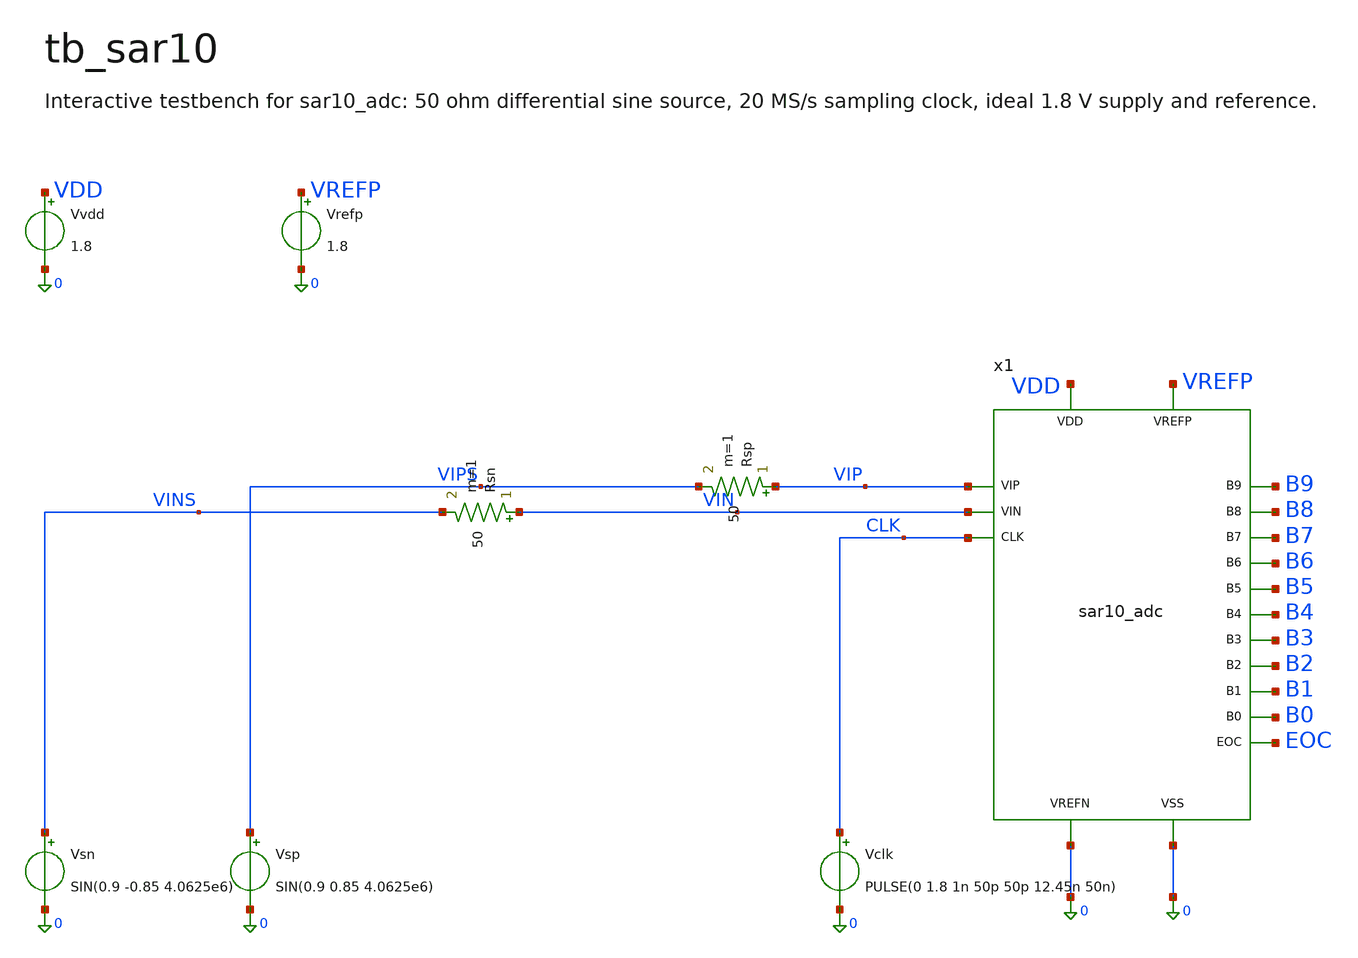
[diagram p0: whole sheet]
** sch_path: xschem/tb_sar10.sch
**.subckt tb_sar10
x1 VIP VIN CLK B9 B8 B7 B6 B5 B4 B3 B2 B1 B0 EOC VDD VREFP 0 0 sar10_adc
Rsp VIP VIPS 50 m=1
Rsn VIN VINS 50 m=1
Vsp VIPS 0 SIN(0.9 0.85 4.0625e6)
Vsn VINS 0 SIN(0.9 -0.85 4.0625e6)
Vclk CLK 0 PULSE(0 1.8 1n 50p 50p 12.45n 50n)
Vvdd VDD 0 1.8
.save i(vvdd)
Vrefp VREFP 0 1.8
.save i(vrefp)
**** begin user architecture code

* sar10_adc bench: 16 conversions of a 4.0625 MHz sine at 20 MS/s (CLK high = sample).
* Netlist + Simulate from xschem.  Corner on the .lib line, temperature on .temp.
* For ENOB / corners / power use the flow instead:  python3 gen/flow.py fft --out sim/x --N 256 --M
*+ 31

.lib /foss/pdks/sky130A/libs.tech/ngspice/sky130.lib.spice tt
.include /foss/pdks/sky130A/libs.ref/sky130_fd_sc_hd/spice/sky130_fd_sc_hd.spice
.include /foss/pdks/sky130A/libs.ref/sky130_fd_pr/spice/sky130_fd_pr__cap_vpp_01p8x01p8_m1m2_noshield.model.spice
.temp 27
.option reltol=2e-4 abstol=1e-13 vntol=1e-7 chgtol=1e-16 method=gear klu rshunt=1e15
.save v(vip) v(vin) v(clk) v(eoc) v(b9) v(b8) v(b7) v(b6) v(b5) v(b4) v(b3) v(b2) v(b1) v(b0)
.save v(x1.topp) v(x1.topn) v(x1.clkc) v(x1.outp) v(x1.outn) i(vvdd) i(vrefp)
.tran 20p 851n 0 40p uic

.control
  run
  let msbs = 512*(v(b9) gt 0.9) + 256*(v(b8) gt 0.9) + 128*(v(b7) gt 0.9) + 64*(v(b6) gt 0.9) +
+ 32*(v(b5) gt 0.9)
  let code = msbs + 16*(v(b4) gt 0.9) + 8*(v(b3) gt 0.9) + 4*(v(b2) gt 0.9) + 2*(v(b1) gt 0.9) +
+ (v(b0) gt 0.9)
  let vd = v(vip) - v(vin)
  meas tran i_vdd AVG i(vvdd) FROM=51n TO=851n
  meas tran i_ref AVG i(vrefp) FROM=51n TO=851n
  let p_uw = -1.8e6*(i_vdd + i_ref)
  echo total power $&p_uw uW at 20 MS/s
  plot code
  plot vd v(eoc) v(clk)
  plot v(x1.topp) v(x1.topn) v(x1.clkc) xlimit 60n 80n
.endc


**** end user architecture code
**.ends

* expanding   symbol:  sar10_adc.sym # of pins=18
** sym_path: xschem/sar10_adc.sym
** sch_path: xschem/sar10_adc.sch
.subckt sar10_adc VIP VIN CLK B9 B8 B7 B6 B5 B4 B3 B2 B1 B0 EOC VDD VREFP VREFN VSS
*.ipin VIP
*.ipin VIN
*.ipin CLK
*.opin EOC
*.opin B9
*.opin B8
*.opin B7
*.opin B6
*.opin B5
*.opin B4
*.opin B3
*.opin B2
*.opin B1
*.opin B0
*.iopin VDD
*.iopin VREFP
*.iopin VREFN
*.iopin VSS
* noconn #net1
* noconn #net2
* noconn #net3
* noconn #net4
* noconn #net5
* noconn #net6
* noconn #net7
* noconn #net8
* noconn #net9
* noconn #net10
* noconn #net11
* noconn #net12
* noconn #net13
XBSP VIP TOPP VDD SAMP VSS sar10_boot
XBSN VIN TOPN VDD SAMP VSS sar10_boot
XDP1 DP1 DNB1 TOPP VDD VREFP VREFN VSS sar10_dac128
XDN1 DN1 DPB1 TOPN VDD VREFP VREFN VSS sar10_dac128
XDP2 DP2 DNB2 TOPP VDD VREFP VREFN VSS sar10_dac64
XDN2 DN2 DPB2 TOPN VDD VREFP VREFN VSS sar10_dac64
XDP3 DP3 DNB3 TOPP VDD VREFP VREFN VSS sar10_dac32
XDN3 DN3 DPB3 TOPN VDD VREFP VREFN VSS sar10_dac32
XDP4 DP4 DNB4 TOPP VDD VREFP VREFN VSS sar10_dac16
XDN4 DN4 DPB4 TOPN VDD VREFP VREFN VSS sar10_dac16
XDP5 DP5 DNB5 TOPP VDD VREFP VREFN VSS sar10_dac8
XDN5 DN5 DPB5 TOPN VDD VREFP VREFN VSS sar10_dac8
XDP6 DP6 DNB6 TOPP VDD VREFP VREFN VSS sar10_dac4
XDN6 DN6 DPB6 TOPN VDD VREFP VREFN VSS sar10_dac4
XDP7 DP7 DNB7 TOPP VDD VREFP VREFN VSS sar10_dac2
XDN7 DN7 DPB7 TOPN VDD VREFP VREFN VSS sar10_dac2
XDP8 DP8 DNB8 TOPP VDD VREFP VREFN VSS sar10_dac1
XDN8 DN8 DPB8 TOPN VDD VREFP VREFN VSS sar10_dac1
XDP9 DP9 DNB9 TOPP VDD VREFP VREFN VSS sar10_dac1
XDN9 TOPN VREFP VREFN VSS sar10_dacdum
XCMP TOPP TOPN CLKC OUTP OUTN VDD VSS sar10_comp
XCTL OUTP OUTN CLK DEC10 CLKC QP QN VALIDB RSTB SAMP EOC VDD VSS sar10_ctrl
XS1 RSTB QP QN VALIDB RSTB EOC T1 net1 DP1 DPB1 DN1 DNB1 B9 VDD VSS sar10_slice
XS2 T1 QP QN VALIDB RSTB EOC T2 net2 DP2 DPB2 DN2 DNB2 B8 VDD VSS sar10_slice
XS3 T2 QP QN VALIDB RSTB EOC T3 net3 DP3 DPB3 DN3 DNB3 B7 VDD VSS sar10_slice
XS4 T3 QP QN VALIDB RSTB EOC T4 net4 DP4 DPB4 DN4 DNB4 B6 VDD VSS sar10_slice
XS5 T4 QP QN VALIDB RSTB EOC T5 net5 DP5 DPB5 DN5 DNB5 B5 VDD VSS sar10_slice
XS6 T5 QP QN VALIDB RSTB EOC T6 net6 DP6 DPB6 DN6 DNB6 B4 VDD VSS sar10_slice
XS7 T6 QP QN VALIDB RSTB EOC T7 net7 DP7 DPB7 DN7 DNB7 B3 VDD VSS sar10_slice
XS8 T7 QP QN VALIDB RSTB EOC T8 net8 DP8 DPB8 DN8 DNB8 B2 VDD VSS sar10_slice
XS9 T8 QP QN VALIDB RSTB EOC T9 net9 DP9 DPB9 DN9 DNB9 B1 VDD VSS sar10_slice
XS10 T9 QP QN VALIDB RSTB EOC net13 DEC10 DP10 net10 net11 net12 B0 VDD VSS sar10_slice
.ends


* expanding   symbol:  sar10_boot.sym # of pins=5
** sym_path: xschem/sar10_boot.sym
** sch_path: xschem/sar10_boot.sch
.subckt sar10_boot VIN VOUT VDD CK VSS
*.ipin CK
*.ipin VIN
*.opin VOUT
*.iopin VDD
*.iopin VSS
XMPI CKB CK VDD VDD sky130_fd_pr__pfet_01v8 L=0.15 W=6 nf=1 ad='int((1 + 1)/2) * 6 / 1 * 0.29' as='int((1 + 2)/2) * 6 / 1 * 0.29'
+ pd='2*int((1 + 1)/2) * (6 / 1 + 0.29)' ps='2*int((1 + 2)/2) * (6 / 1 + 0.29)' nrd='0.29 / 6 ' nrs='0.29 / 6 '
+ sa=0 sb=0 sd=0 mult=1 m=1
XMNI CKB CK VSS VSS sky130_fd_pr__nfet_01v8 L=0.15 W=3 nf=1 ad='int((1 + 1)/2) * 3 / 1 * 0.29' as='int((1 + 2)/2) * 3 / 1 * 0.29'
+ pd='2*int((1 + 1)/2) * (3 / 1 + 0.29)' ps='2*int((1 + 2)/2) * (3 / 1 + 0.29)' nrd='0.29 / 3 ' nrs='0.29 / 3 '
+ sa=0 sb=0 sd=0 mult=1 m=1
XMP1 TOP G VDD TOP sky130_fd_pr__pfet_01v8 L=0.15 W=2 nf=1 ad='int((1 + 1)/2) * 2 / 1 * 0.29' as='int((1 + 2)/2) * 2 / 1 * 0.29'
+ pd='2*int((1 + 1)/2) * (2 / 1 + 0.29)' ps='2*int((1 + 2)/2) * (2 / 1 + 0.29)' nrd='0.29 / 2 ' nrs='0.29 / 2 '
+ sa=0 sb=0 sd=0 mult=1 m=1
XCB TOP BOT sky130_fd_pr__cap_mim_m3_1 W=9 L=9 MF=1 m=1
XMN1 BOT CKB VSS VSS sky130_fd_pr__nfet_01v8 L=0.15 W=2 nf=1 ad='int((1 + 1)/2) * 2 / 1 * 0.29' as='int((1 + 2)/2) * 2 / 1 * 0.29'
+ pd='2*int((1 + 1)/2) * (2 / 1 + 0.29)' ps='2*int((1 + 2)/2) * (2 / 1 + 0.29)' nrd='0.29 / 2 ' nrs='0.29 / 2 '
+ sa=0 sb=0 sd=0 mult=1 m=1
XMP4 Z CK VDD VDD sky130_fd_pr__pfet_01v8 L=0.15 W=6 nf=1 ad='int((1 + 1)/2) * 6 / 1 * 0.29' as='int((1 + 2)/2) * 6 / 1 * 0.29'
+ pd='2*int((1 + 1)/2) * (6 / 1 + 0.29)' ps='2*int((1 + 2)/2) * (6 / 1 + 0.29)' nrd='0.29 / 6 ' nrs='0.29 / 6 '
+ sa=0 sb=0 sd=0 mult=1 m=1
XMN4 Z CK BOT VSS sky130_fd_pr__nfet_01v8 L=0.15 W=1 nf=1 ad='int((1 + 1)/2) * 1 / 1 * 0.29' as='int((1 + 2)/2) * 1 / 1 * 0.29'
+ pd='2*int((1 + 1)/2) * (1 / 1 + 0.29)' ps='2*int((1 + 2)/2) * (1 / 1 + 0.29)' nrd='0.29 / 1 ' nrs='0.29 / 1 '
+ sa=0 sb=0 sd=0 mult=1 m=1
XMN4B Z G BOT VSS sky130_fd_pr__nfet_01v8 L=0.15 W=1 nf=1 ad='int((1 + 1)/2) * 1 / 1 * 0.29' as='int((1 + 2)/2) * 1 / 1 * 0.29'
+ pd='2*int((1 + 1)/2) * (1 / 1 + 0.29)' ps='2*int((1 + 2)/2) * (1 / 1 + 0.29)' nrd='0.29 / 1 ' nrs='0.29 / 1 '
+ sa=0 sb=0 sd=0 mult=1 m=1
XMP2 G Z TOP TOP sky130_fd_pr__pfet_01v8 L=0.15 W=4 nf=1 ad='int((1 + 1)/2) * 4 / 1 * 0.29' as='int((1 + 2)/2) * 4 / 1 * 0.29'
+ pd='2*int((1 + 1)/2) * (4 / 1 + 0.29)' ps='2*int((1 + 2)/2) * (4 / 1 + 0.29)' nrd='0.29 / 4 ' nrs='0.29 / 4 '
+ sa=0 sb=0 sd=0 mult=1 m=1
XMN3 BOT G VIN VSS sky130_fd_pr__nfet_01v8 L=0.15 W=4 nf=1 ad='int((1 + 1)/2) * 4 / 1 * 0.29' as='int((1 + 2)/2) * 4 / 1 * 0.29'
+ pd='2*int((1 + 1)/2) * (4 / 1 + 0.29)' ps='2*int((1 + 2)/2) * (4 / 1 + 0.29)' nrd='0.29 / 4 ' nrs='0.29 / 4 '
+ sa=0 sb=0 sd=0 mult=1 m=1
XMN2A G VDD GX VSS sky130_fd_pr__nfet_01v8 L=0.15 W=12 nf=1 ad='int((1 + 1)/2) * 12 / 1 * 0.29' as='int((1 + 2)/2) * 12 / 1 * 0.29'
+ pd='2*int((1 + 1)/2) * (12 / 1 + 0.29)' ps='2*int((1 + 2)/2) * (12 / 1 + 0.29)' nrd='0.29 / 12 ' nrs='0.29 / 12 '
+ sa=0 sb=0 sd=0 mult=1 m=1
XMN2 GX CKB VSS VSS sky130_fd_pr__nfet_01v8 L=0.15 W=12 nf=1 ad='int((1 + 1)/2) * 12 / 1 * 0.29' as='int((1 + 2)/2) * 12 / 1 * 0.29'
+ pd='2*int((1 + 1)/2) * (12 / 1 + 0.29)' ps='2*int((1 + 2)/2) * (12 / 1 + 0.29)' nrd='0.29 / 12 ' nrs='0.29 / 12 '
+ sa=0 sb=0 sd=0 mult=1 m=1
XMSW VOUT G VIN VSS sky130_fd_pr__nfet_01v8 L=0.15 W=5 nf=2 ad='int((2 + 1)/2) * 5 / 2 * 0.29' as='int((2 + 2)/2) * 5 / 2 * 0.29'
+ pd='2*int((2 + 1)/2) * (5 / 2 + 0.29)' ps='2*int((2 + 2)/2) * (5 / 2 + 0.29)' nrd='0.29 / 5 ' nrs='0.29 / 5 '
+ sa=0 sb=0 sd=0 mult=1 m=1
.ends


* expanding   symbol:  sar10_dac128.sym # of pins=7
** sym_path: xschem/sar10_dac128.sym
** sch_path: xschem/sar10_dac128.sch
.subckt sar10_dac128 DH DL TOP VDD VREFP VREFN VSS
*.ipin DH
*.ipin DL
*.iopin TOP
*.iopin VDD
*.iopin VREFP
*.iopin VREFN
*.iopin VSS
XMP3H BH DH VREFP VREFP sky130_fd_pr__pfet_01v8 L=0.15 W=14.4 nf=3 ad='int((3 + 1)/2) * 14.4 / 3 * 0.29'
+ as='int((3 + 2)/2) * 14.4 / 3 * 0.29' pd='2*int((3 + 1)/2) * (14.4 / 3 + 0.29)' ps='2*int((3 + 2)/2) * (14.4 / 3 + 0.29)'
+ nrd='0.29 / 14.4 ' nrs='0.29 / 14.4 ' sa=0 sb=0 sd=0 mult=1 m=1
XMN3H BH DH VREFN VREFN sky130_fd_pr__nfet_01v8 L=0.15 W=5.76 nf=2 ad='int((2 + 1)/2) * 5.76 / 2 * 0.29'
+ as='int((2 + 2)/2) * 5.76 / 2 * 0.29' pd='2*int((2 + 1)/2) * (5.76 / 2 + 0.29)' ps='2*int((2 + 2)/2) * (5.76 / 2 + 0.29)'
+ nrd='0.29 / 5.76 ' nrs='0.29 / 5.76 ' sa=0 sb=0 sd=0 mult=1 m=1
XMP3L BL DL VREFP VREFP sky130_fd_pr__pfet_01v8 L=0.15 W=14.4 nf=3 ad='int((3 + 1)/2) * 14.4 / 3 * 0.29'
+ as='int((3 + 2)/2) * 14.4 / 3 * 0.29' pd='2*int((3 + 1)/2) * (14.4 / 3 + 0.29)' ps='2*int((3 + 2)/2) * (14.4 / 3 + 0.29)'
+ nrd='0.29 / 14.4 ' nrs='0.29 / 14.4 ' sa=0 sb=0 sd=0 mult=1 m=1
XMN3L BL DL VREFN VREFN sky130_fd_pr__nfet_01v8 L=0.15 W=5.76 nf=2 ad='int((2 + 1)/2) * 5.76 / 2 * 0.29'
+ as='int((2 + 2)/2) * 5.76 / 2 * 0.29' pd='2*int((2 + 1)/2) * (5.76 / 2 + 0.29)' ps='2*int((2 + 2)/2) * (5.76 / 2 + 0.29)'
+ nrd='0.29 / 5.76 ' nrs='0.29 / 5.76 ' sa=0 sb=0 sd=0 mult=1 m=1
XCH BH TOP VSS sky130_fd_pr__cap_vpp_01p8x01p8_m1m2_noshield mult=128 m=128
XCL BL TOP VSS sky130_fd_pr__cap_vpp_01p8x01p8_m1m2_noshield mult=128 m=128
.ends


* expanding   symbol:  sar10_dac64.sym # of pins=7
** sym_path: xschem/sar10_dac64.sym
** sch_path: xschem/sar10_dac64.sch
.subckt sar10_dac64 DH DL TOP VDD VREFP VREFN VSS
*.ipin DH
*.ipin DL
*.iopin TOP
*.iopin VDD
*.iopin VREFP
*.iopin VREFN
*.iopin VSS
XMP3H BH DH VREFP VREFP sky130_fd_pr__pfet_01v8 L=0.15 W=7.2 nf=2 ad='int((2 + 1)/2) * 7.2 / 2 * 0.29'
+ as='int((2 + 2)/2) * 7.2 / 2 * 0.29' pd='2*int((2 + 1)/2) * (7.2 / 2 + 0.29)' ps='2*int((2 + 2)/2) * (7.2 / 2 + 0.29)'
+ nrd='0.29 / 7.2 ' nrs='0.29 / 7.2 ' sa=0 sb=0 sd=0 mult=1 m=1
XMN3H BH DH VREFN VREFN sky130_fd_pr__nfet_01v8 L=0.15 W=2.88 nf=1 ad='int((1 + 1)/2) * 2.88 / 1 * 0.29'
+ as='int((1 + 2)/2) * 2.88 / 1 * 0.29' pd='2*int((1 + 1)/2) * (2.88 / 1 + 0.29)' ps='2*int((1 + 2)/2) * (2.88 / 1 + 0.29)'
+ nrd='0.29 / 2.88 ' nrs='0.29 / 2.88 ' sa=0 sb=0 sd=0 mult=1 m=1
XMP3L BL DL VREFP VREFP sky130_fd_pr__pfet_01v8 L=0.15 W=7.2 nf=2 ad='int((2 + 1)/2) * 7.2 / 2 * 0.29'
+ as='int((2 + 2)/2) * 7.2 / 2 * 0.29' pd='2*int((2 + 1)/2) * (7.2 / 2 + 0.29)' ps='2*int((2 + 2)/2) * (7.2 / 2 + 0.29)'
+ nrd='0.29 / 7.2 ' nrs='0.29 / 7.2 ' sa=0 sb=0 sd=0 mult=1 m=1
XMN3L BL DL VREFN VREFN sky130_fd_pr__nfet_01v8 L=0.15 W=2.88 nf=1 ad='int((1 + 1)/2) * 2.88 / 1 * 0.29'
+ as='int((1 + 2)/2) * 2.88 / 1 * 0.29' pd='2*int((1 + 1)/2) * (2.88 / 1 + 0.29)' ps='2*int((1 + 2)/2) * (2.88 / 1 + 0.29)'
+ nrd='0.29 / 2.88 ' nrs='0.29 / 2.88 ' sa=0 sb=0 sd=0 mult=1 m=1
XCH BH TOP VSS sky130_fd_pr__cap_vpp_01p8x01p8_m1m2_noshield mult=64 m=64
XCL BL TOP VSS sky130_fd_pr__cap_vpp_01p8x01p8_m1m2_noshield mult=64 m=64
.ends


* expanding   symbol:  sar10_dac32.sym # of pins=7
** sym_path: xschem/sar10_dac32.sym
** sch_path: xschem/sar10_dac32.sch
.subckt sar10_dac32 DH DL TOP VDD VREFP VREFN VSS
*.ipin DH
*.ipin DL
*.iopin TOP
*.iopin VDD
*.iopin VREFP
*.iopin VREFN
*.iopin VSS
XMP3H BH DH VREFP VREFP sky130_fd_pr__pfet_01v8 L=0.15 W=3.6 nf=1 ad='int((1 + 1)/2) * 3.6 / 1 * 0.29'
+ as='int((1 + 2)/2) * 3.6 / 1 * 0.29' pd='2*int((1 + 1)/2) * (3.6 / 1 + 0.29)' ps='2*int((1 + 2)/2) * (3.6 / 1 + 0.29)'
+ nrd='0.29 / 3.6 ' nrs='0.29 / 3.6 ' sa=0 sb=0 sd=0 mult=1 m=1
XMN3H BH DH VREFN VREFN sky130_fd_pr__nfet_01v8 L=0.15 W=1.44 nf=1 ad='int((1 + 1)/2) * 1.44 / 1 * 0.29'
+ as='int((1 + 2)/2) * 1.44 / 1 * 0.29' pd='2*int((1 + 1)/2) * (1.44 / 1 + 0.29)' ps='2*int((1 + 2)/2) * (1.44 / 1 + 0.29)'
+ nrd='0.29 / 1.44 ' nrs='0.29 / 1.44 ' sa=0 sb=0 sd=0 mult=1 m=1
XMP3L BL DL VREFP VREFP sky130_fd_pr__pfet_01v8 L=0.15 W=3.6 nf=1 ad='int((1 + 1)/2) * 3.6 / 1 * 0.29'
+ as='int((1 + 2)/2) * 3.6 / 1 * 0.29' pd='2*int((1 + 1)/2) * (3.6 / 1 + 0.29)' ps='2*int((1 + 2)/2) * (3.6 / 1 + 0.29)'
+ nrd='0.29 / 3.6 ' nrs='0.29 / 3.6 ' sa=0 sb=0 sd=0 mult=1 m=1
XMN3L BL DL VREFN VREFN sky130_fd_pr__nfet_01v8 L=0.15 W=1.44 nf=1 ad='int((1 + 1)/2) * 1.44 / 1 * 0.29'
+ as='int((1 + 2)/2) * 1.44 / 1 * 0.29' pd='2*int((1 + 1)/2) * (1.44 / 1 + 0.29)' ps='2*int((1 + 2)/2) * (1.44 / 1 + 0.29)'
+ nrd='0.29 / 1.44 ' nrs='0.29 / 1.44 ' sa=0 sb=0 sd=0 mult=1 m=1
XCH BH TOP VSS sky130_fd_pr__cap_vpp_01p8x01p8_m1m2_noshield mult=32 m=32
XCL BL TOP VSS sky130_fd_pr__cap_vpp_01p8x01p8_m1m2_noshield mult=32 m=32
.ends


* expanding   symbol:  sar10_dac16.sym # of pins=7
** sym_path: xschem/sar10_dac16.sym
** sch_path: xschem/sar10_dac16.sch
.subckt sar10_dac16 DH DL TOP VDD VREFP VREFN VSS
*.ipin DH
*.ipin DL
*.iopin TOP
*.iopin VDD
*.iopin VREFP
*.iopin VREFN
*.iopin VSS
XMP3H BH DH VREFP VREFP sky130_fd_pr__pfet_01v8 L=0.15 W=1.8 nf=1 ad='int((1 + 1)/2) * 1.8 / 1 * 0.29'
+ as='int((1 + 2)/2) * 1.8 / 1 * 0.29' pd='2*int((1 + 1)/2) * (1.8 / 1 + 0.29)' ps='2*int((1 + 2)/2) * (1.8 / 1 + 0.29)'
+ nrd='0.29 / 1.8 ' nrs='0.29 / 1.8 ' sa=0 sb=0 sd=0 mult=1 m=1
XMN3H BH DH VREFN VREFN sky130_fd_pr__nfet_01v8 L=0.15 W=0.72 nf=1 ad='int((1 + 1)/2) * 0.72 / 1 * 0.29'
+ as='int((1 + 2)/2) * 0.72 / 1 * 0.29' pd='2*int((1 + 1)/2) * (0.72 / 1 + 0.29)' ps='2*int((1 + 2)/2) * (0.72 / 1 + 0.29)'
+ nrd='0.29 / 0.72 ' nrs='0.29 / 0.72 ' sa=0 sb=0 sd=0 mult=1 m=1
XMP3L BL DL VREFP VREFP sky130_fd_pr__pfet_01v8 L=0.15 W=1.8 nf=1 ad='int((1 + 1)/2) * 1.8 / 1 * 0.29'
+ as='int((1 + 2)/2) * 1.8 / 1 * 0.29' pd='2*int((1 + 1)/2) * (1.8 / 1 + 0.29)' ps='2*int((1 + 2)/2) * (1.8 / 1 + 0.29)'
+ nrd='0.29 / 1.8 ' nrs='0.29 / 1.8 ' sa=0 sb=0 sd=0 mult=1 m=1
XMN3L BL DL VREFN VREFN sky130_fd_pr__nfet_01v8 L=0.15 W=0.72 nf=1 ad='int((1 + 1)/2) * 0.72 / 1 * 0.29'
+ as='int((1 + 2)/2) * 0.72 / 1 * 0.29' pd='2*int((1 + 1)/2) * (0.72 / 1 + 0.29)' ps='2*int((1 + 2)/2) * (0.72 / 1 + 0.29)'
+ nrd='0.29 / 0.72 ' nrs='0.29 / 0.72 ' sa=0 sb=0 sd=0 mult=1 m=1
XCH BH TOP VSS sky130_fd_pr__cap_vpp_01p8x01p8_m1m2_noshield mult=16 m=16
XCL BL TOP VSS sky130_fd_pr__cap_vpp_01p8x01p8_m1m2_noshield mult=16 m=16
.ends


* expanding   symbol:  sar10_dac8.sym # of pins=7
** sym_path: xschem/sar10_dac8.sym
** sch_path: xschem/sar10_dac8.sch
.subckt sar10_dac8 DH DL TOP VDD VREFP VREFN VSS
*.ipin DH
*.ipin DL
*.iopin TOP
*.iopin VDD
*.iopin VREFP
*.iopin VREFN
*.iopin VSS
XMP3H BH DH VREFP VREFP sky130_fd_pr__pfet_01v8 L=0.15 W=1.05 nf=1 ad='int((1 + 1)/2) * 1.05 / 1 * 0.29'
+ as='int((1 + 2)/2) * 1.05 / 1 * 0.29' pd='2*int((1 + 1)/2) * (1.05 / 1 + 0.29)' ps='2*int((1 + 2)/2) * (1.05 / 1 + 0.29)'
+ nrd='0.29 / 1.05 ' nrs='0.29 / 1.05 ' sa=0 sb=0 sd=0 mult=1 m=1
XMN3H BH DH VREFN VREFN sky130_fd_pr__nfet_01v8 L=0.15 W=0.42 nf=1 ad='int((1 + 1)/2) * 0.42 / 1 * 0.29'
+ as='int((1 + 2)/2) * 0.42 / 1 * 0.29' pd='2*int((1 + 1)/2) * (0.42 / 1 + 0.29)' ps='2*int((1 + 2)/2) * (0.42 / 1 + 0.29)'
+ nrd='0.29 / 0.42 ' nrs='0.29 / 0.42 ' sa=0 sb=0 sd=0 mult=1 m=1
XMP3L BL DL VREFP VREFP sky130_fd_pr__pfet_01v8 L=0.15 W=1.05 nf=1 ad='int((1 + 1)/2) * 1.05 / 1 * 0.29'
+ as='int((1 + 2)/2) * 1.05 / 1 * 0.29' pd='2*int((1 + 1)/2) * (1.05 / 1 + 0.29)' ps='2*int((1 + 2)/2) * (1.05 / 1 + 0.29)'
+ nrd='0.29 / 1.05 ' nrs='0.29 / 1.05 ' sa=0 sb=0 sd=0 mult=1 m=1
XMN3L BL DL VREFN VREFN sky130_fd_pr__nfet_01v8 L=0.15 W=0.42 nf=1 ad='int((1 + 1)/2) * 0.42 / 1 * 0.29'
+ as='int((1 + 2)/2) * 0.42 / 1 * 0.29' pd='2*int((1 + 1)/2) * (0.42 / 1 + 0.29)' ps='2*int((1 + 2)/2) * (0.42 / 1 + 0.29)'
+ nrd='0.29 / 0.42 ' nrs='0.29 / 0.42 ' sa=0 sb=0 sd=0 mult=1 m=1
XCH BH TOP VSS sky130_fd_pr__cap_vpp_01p8x01p8_m1m2_noshield mult=8 m=8
XCL BL TOP VSS sky130_fd_pr__cap_vpp_01p8x01p8_m1m2_noshield mult=8 m=8
.ends


* expanding   symbol:  sar10_dac4.sym # of pins=7
** sym_path: xschem/sar10_dac4.sym
** sch_path: xschem/sar10_dac4.sch
.subckt sar10_dac4 DH DL TOP VDD VREFP VREFN VSS
*.ipin DH
*.ipin DL
*.iopin TOP
*.iopin VDD
*.iopin VREFP
*.iopin VREFN
*.iopin VSS
XMP3H BH DH VREFP VREFP sky130_fd_pr__pfet_01v8 L=0.15 W=1.05 nf=1 ad='int((1 + 1)/2) * 1.05 / 1 * 0.29'
+ as='int((1 + 2)/2) * 1.05 / 1 * 0.29' pd='2*int((1 + 1)/2) * (1.05 / 1 + 0.29)' ps='2*int((1 + 2)/2) * (1.05 / 1 + 0.29)'
+ nrd='0.29 / 1.05 ' nrs='0.29 / 1.05 ' sa=0 sb=0 sd=0 mult=1 m=1
XMN3H BH DH VREFN VREFN sky130_fd_pr__nfet_01v8 L=0.15 W=0.42 nf=1 ad='int((1 + 1)/2) * 0.42 / 1 * 0.29'
+ as='int((1 + 2)/2) * 0.42 / 1 * 0.29' pd='2*int((1 + 1)/2) * (0.42 / 1 + 0.29)' ps='2*int((1 + 2)/2) * (0.42 / 1 + 0.29)'
+ nrd='0.29 / 0.42 ' nrs='0.29 / 0.42 ' sa=0 sb=0 sd=0 mult=1 m=1
XMP3L BL DL VREFP VREFP sky130_fd_pr__pfet_01v8 L=0.15 W=1.05 nf=1 ad='int((1 + 1)/2) * 1.05 / 1 * 0.29'
+ as='int((1 + 2)/2) * 1.05 / 1 * 0.29' pd='2*int((1 + 1)/2) * (1.05 / 1 + 0.29)' ps='2*int((1 + 2)/2) * (1.05 / 1 + 0.29)'
+ nrd='0.29 / 1.05 ' nrs='0.29 / 1.05 ' sa=0 sb=0 sd=0 mult=1 m=1
XMN3L BL DL VREFN VREFN sky130_fd_pr__nfet_01v8 L=0.15 W=0.42 nf=1 ad='int((1 + 1)/2) * 0.42 / 1 * 0.29'
+ as='int((1 + 2)/2) * 0.42 / 1 * 0.29' pd='2*int((1 + 1)/2) * (0.42 / 1 + 0.29)' ps='2*int((1 + 2)/2) * (0.42 / 1 + 0.29)'
+ nrd='0.29 / 0.42 ' nrs='0.29 / 0.42 ' sa=0 sb=0 sd=0 mult=1 m=1
XCH BH TOP VSS sky130_fd_pr__cap_vpp_01p8x01p8_m1m2_noshield mult=4 m=4
XCL BL TOP VSS sky130_fd_pr__cap_vpp_01p8x01p8_m1m2_noshield mult=4 m=4
.ends


* expanding   symbol:  sar10_dac2.sym # of pins=7
** sym_path: xschem/sar10_dac2.sym
** sch_path: xschem/sar10_dac2.sch
.subckt sar10_dac2 DH DL TOP VDD VREFP VREFN VSS
*.ipin DH
*.ipin DL
*.iopin TOP
*.iopin VDD
*.iopin VREFP
*.iopin VREFN
*.iopin VSS
XMP3H BH DH VREFP VREFP sky130_fd_pr__pfet_01v8 L=0.15 W=1.05 nf=1 ad='int((1 + 1)/2) * 1.05 / 1 * 0.29'
+ as='int((1 + 2)/2) * 1.05 / 1 * 0.29' pd='2*int((1 + 1)/2) * (1.05 / 1 + 0.29)' ps='2*int((1 + 2)/2) * (1.05 / 1 + 0.29)'
+ nrd='0.29 / 1.05 ' nrs='0.29 / 1.05 ' sa=0 sb=0 sd=0 mult=1 m=1
XMN3H BH DH VREFN VREFN sky130_fd_pr__nfet_01v8 L=0.15 W=0.42 nf=1 ad='int((1 + 1)/2) * 0.42 / 1 * 0.29'
+ as='int((1 + 2)/2) * 0.42 / 1 * 0.29' pd='2*int((1 + 1)/2) * (0.42 / 1 + 0.29)' ps='2*int((1 + 2)/2) * (0.42 / 1 + 0.29)'
+ nrd='0.29 / 0.42 ' nrs='0.29 / 0.42 ' sa=0 sb=0 sd=0 mult=1 m=1
XMP3L BL DL VREFP VREFP sky130_fd_pr__pfet_01v8 L=0.15 W=1.05 nf=1 ad='int((1 + 1)/2) * 1.05 / 1 * 0.29'
+ as='int((1 + 2)/2) * 1.05 / 1 * 0.29' pd='2*int((1 + 1)/2) * (1.05 / 1 + 0.29)' ps='2*int((1 + 2)/2) * (1.05 / 1 + 0.29)'
+ nrd='0.29 / 1.05 ' nrs='0.29 / 1.05 ' sa=0 sb=0 sd=0 mult=1 m=1
XMN3L BL DL VREFN VREFN sky130_fd_pr__nfet_01v8 L=0.15 W=0.42 nf=1 ad='int((1 + 1)/2) * 0.42 / 1 * 0.29'
+ as='int((1 + 2)/2) * 0.42 / 1 * 0.29' pd='2*int((1 + 1)/2) * (0.42 / 1 + 0.29)' ps='2*int((1 + 2)/2) * (0.42 / 1 + 0.29)'
+ nrd='0.29 / 0.42 ' nrs='0.29 / 0.42 ' sa=0 sb=0 sd=0 mult=1 m=1
XCH BH TOP VSS sky130_fd_pr__cap_vpp_01p8x01p8_m1m2_noshield mult=2 m=2
XCL BL TOP VSS sky130_fd_pr__cap_vpp_01p8x01p8_m1m2_noshield mult=2 m=2
.ends


* expanding   symbol:  sar10_dac1.sym # of pins=7
** sym_path: xschem/sar10_dac1.sym
** sch_path: xschem/sar10_dac1.sch
.subckt sar10_dac1 DH DL TOP VDD VREFP VREFN VSS
*.ipin DH
*.ipin DL
*.iopin TOP
*.iopin VDD
*.iopin VREFP
*.iopin VREFN
*.iopin VSS
XMP3H BH DH VREFP VREFP sky130_fd_pr__pfet_01v8 L=0.15 W=1.05 nf=1 ad='int((1 + 1)/2) * 1.05 / 1 * 0.29'
+ as='int((1 + 2)/2) * 1.05 / 1 * 0.29' pd='2*int((1 + 1)/2) * (1.05 / 1 + 0.29)' ps='2*int((1 + 2)/2) * (1.05 / 1 + 0.29)'
+ nrd='0.29 / 1.05 ' nrs='0.29 / 1.05 ' sa=0 sb=0 sd=0 mult=1 m=1
XMN3H BH DH VREFN VREFN sky130_fd_pr__nfet_01v8 L=0.15 W=0.42 nf=1 ad='int((1 + 1)/2) * 0.42 / 1 * 0.29'
+ as='int((1 + 2)/2) * 0.42 / 1 * 0.29' pd='2*int((1 + 1)/2) * (0.42 / 1 + 0.29)' ps='2*int((1 + 2)/2) * (0.42 / 1 + 0.29)'
+ nrd='0.29 / 0.42 ' nrs='0.29 / 0.42 ' sa=0 sb=0 sd=0 mult=1 m=1
XMP3L BL DL VREFP VREFP sky130_fd_pr__pfet_01v8 L=0.15 W=1.05 nf=1 ad='int((1 + 1)/2) * 1.05 / 1 * 0.29'
+ as='int((1 + 2)/2) * 1.05 / 1 * 0.29' pd='2*int((1 + 1)/2) * (1.05 / 1 + 0.29)' ps='2*int((1 + 2)/2) * (1.05 / 1 + 0.29)'
+ nrd='0.29 / 1.05 ' nrs='0.29 / 1.05 ' sa=0 sb=0 sd=0 mult=1 m=1
XMN3L BL DL VREFN VREFN sky130_fd_pr__nfet_01v8 L=0.15 W=0.42 nf=1 ad='int((1 + 1)/2) * 0.42 / 1 * 0.29'
+ as='int((1 + 2)/2) * 0.42 / 1 * 0.29' pd='2*int((1 + 1)/2) * (0.42 / 1 + 0.29)' ps='2*int((1 + 2)/2) * (0.42 / 1 + 0.29)'
+ nrd='0.29 / 0.42 ' nrs='0.29 / 0.42 ' sa=0 sb=0 sd=0 mult=1 m=1
XCH BH TOP VSS sky130_fd_pr__cap_vpp_01p8x01p8_m1m2_noshield mult=1 m=1
XCL BL TOP VSS sky130_fd_pr__cap_vpp_01p8x01p8_m1m2_noshield mult=1 m=1
.ends


* expanding   symbol:  sar10_dacdum.sym # of pins=4
** sym_path: xschem/sar10_dacdum.sym
** sch_path: xschem/sar10_dacdum.sch
.subckt sar10_dacdum TOP VREFP VREFN VSS
*.iopin TOP
*.iopin VREFP
*.iopin VREFN
*.iopin VSS
XCH VREFP TOP VSS sky130_fd_pr__cap_vpp_01p8x01p8_m1m2_noshield mult=1 m=1
XCL VREFN TOP VSS sky130_fd_pr__cap_vpp_01p8x01p8_m1m2_noshield mult=1 m=1
.ends


* expanding   symbol:  sar10_comp.sym # of pins=7
** sym_path: xschem/sar10_comp.sym
** sch_path: xschem/sar10_comp.sch
.subckt sar10_comp INP INN CLK OUTP OUTN VDD VSS
*.ipin INP
*.ipin INN
*.ipin CLK
*.opin OUTP
*.opin OUTN
*.iopin VDD
*.iopin VSS
XM0 TAIL CLK VSS VSS sky130_fd_pr__nfet_01v8 L=0.15 W=2 nf=1 ad='int((1 + 1)/2) * 2 / 1 * 0.29' as='int((1 + 2)/2) * 2 / 1 * 0.29'
+ pd='2*int((1 + 1)/2) * (2 / 1 + 0.29)' ps='2*int((1 + 2)/2) * (2 / 1 + 0.29)' nrd='0.29 / 2 ' nrs='0.29 / 2 '
+ sa=0 sb=0 sd=0 mult=1 m=1
XM0B TAIL CLK VSS VSS sky130_fd_pr__nfet_01v8 L=0.15 W=2 nf=1 ad='int((1 + 1)/2) * 2 / 1 * 0.29' as='int((1 + 2)/2) * 2 / 1 * 0.29'
+ pd='2*int((1 + 1)/2) * (2 / 1 + 0.29)' ps='2*int((1 + 2)/2) * (2 / 1 + 0.29)' nrd='0.29 / 2 ' nrs='0.29 / 2 '
+ sa=0 sb=0 sd=0 mult=1 m=1
XM1 XN INP TAIL VSS sky130_fd_pr__nfet_01v8 L=0.15 W=4 nf=1 ad='int((1 + 1)/2) * 4 / 1 * 0.29' as='int((1 + 2)/2) * 4 / 1 * 0.29'
+ pd='2*int((1 + 1)/2) * (4 / 1 + 0.29)' ps='2*int((1 + 2)/2) * (4 / 1 + 0.29)' nrd='0.29 / 4 ' nrs='0.29 / 4 '
+ sa=0 sb=0 sd=0 mult=1 m=1
XM2 XP INN TAIL VSS sky130_fd_pr__nfet_01v8 L=0.15 W=4 nf=1 ad='int((1 + 1)/2) * 4 / 1 * 0.29' as='int((1 + 2)/2) * 4 / 1 * 0.29'
+ pd='2*int((1 + 1)/2) * (4 / 1 + 0.29)' ps='2*int((1 + 2)/2) * (4 / 1 + 0.29)' nrd='0.29 / 4 ' nrs='0.29 / 4 '
+ sa=0 sb=0 sd=0 mult=1 m=1
XM3 OUTN OUTP XN VSS sky130_fd_pr__nfet_01v8 L=0.15 W=2 nf=1 ad='int((1 + 1)/2) * 2 / 1 * 0.29' as='int((1 + 2)/2) * 2 / 1 * 0.29'
+ pd='2*int((1 + 1)/2) * (2 / 1 + 0.29)' ps='2*int((1 + 2)/2) * (2 / 1 + 0.29)' nrd='0.29 / 2 ' nrs='0.29 / 2 '
+ sa=0 sb=0 sd=0 mult=1 m=1
XM4 OUTP OUTN XP VSS sky130_fd_pr__nfet_01v8 L=0.15 W=2 nf=1 ad='int((1 + 1)/2) * 2 / 1 * 0.29' as='int((1 + 2)/2) * 2 / 1 * 0.29'
+ pd='2*int((1 + 1)/2) * (2 / 1 + 0.29)' ps='2*int((1 + 2)/2) * (2 / 1 + 0.29)' nrd='0.29 / 2 ' nrs='0.29 / 2 '
+ sa=0 sb=0 sd=0 mult=1 m=1
XM5 OUTN OUTP VDD VDD sky130_fd_pr__pfet_01v8 L=0.15 W=2 nf=1 ad='int((1 + 1)/2) * 2 / 1 * 0.29' as='int((1 + 2)/2) * 2 / 1 * 0.29'
+ pd='2*int((1 + 1)/2) * (2 / 1 + 0.29)' ps='2*int((1 + 2)/2) * (2 / 1 + 0.29)' nrd='0.29 / 2 ' nrs='0.29 / 2 '
+ sa=0 sb=0 sd=0 mult=1 m=1
XM6 OUTP OUTN VDD VDD sky130_fd_pr__pfet_01v8 L=0.15 W=2 nf=1 ad='int((1 + 1)/2) * 2 / 1 * 0.29' as='int((1 + 2)/2) * 2 / 1 * 0.29'
+ pd='2*int((1 + 1)/2) * (2 / 1 + 0.29)' ps='2*int((1 + 2)/2) * (2 / 1 + 0.29)' nrd='0.29 / 2 ' nrs='0.29 / 2 '
+ sa=0 sb=0 sd=0 mult=1 m=1
XM7 OUTN CLK VDD VDD sky130_fd_pr__pfet_01v8 L=0.15 W=1 nf=1 ad='int((1 + 1)/2) * 1 / 1 * 0.29' as='int((1 + 2)/2) * 1 / 1 * 0.29'
+ pd='2*int((1 + 1)/2) * (1 / 1 + 0.29)' ps='2*int((1 + 2)/2) * (1 / 1 + 0.29)' nrd='0.29 / 1 ' nrs='0.29 / 1 '
+ sa=0 sb=0 sd=0 mult=1 m=1
XM8 OUTP CLK VDD VDD sky130_fd_pr__pfet_01v8 L=0.15 W=1 nf=1 ad='int((1 + 1)/2) * 1 / 1 * 0.29' as='int((1 + 2)/2) * 1 / 1 * 0.29'
+ pd='2*int((1 + 1)/2) * (1 / 1 + 0.29)' ps='2*int((1 + 2)/2) * (1 / 1 + 0.29)' nrd='0.29 / 1 ' nrs='0.29 / 1 '
+ sa=0 sb=0 sd=0 mult=1 m=1
XM9 XN CLK VDD VDD sky130_fd_pr__pfet_01v8 L=0.15 W=1 nf=1 ad='int((1 + 1)/2) * 1 / 1 * 0.29' as='int((1 + 2)/2) * 1 / 1 * 0.29'
+ pd='2*int((1 + 1)/2) * (1 / 1 + 0.29)' ps='2*int((1 + 2)/2) * (1 / 1 + 0.29)' nrd='0.29 / 1 ' nrs='0.29 / 1 '
+ sa=0 sb=0 sd=0 mult=1 m=1
XM10 XP CLK VDD VDD sky130_fd_pr__pfet_01v8 L=0.15 W=1 nf=1 ad='int((1 + 1)/2) * 1 / 1 * 0.29' as='int((1 + 2)/2) * 1 / 1 * 0.29'
+ pd='2*int((1 + 1)/2) * (1 / 1 + 0.29)' ps='2*int((1 + 2)/2) * (1 / 1 + 0.29)' nrd='0.29 / 1 ' nrs='0.29 / 1 '
+ sa=0 sb=0 sd=0 mult=1 m=1
.ends


* expanding   symbol:  sar10_ctrl.sym # of pins=13
** sym_path: xschem/sar10_ctrl.sym
** sch_path: xschem/sar10_ctrl.sch
.subckt sar10_ctrl OUTP OUTN CLKS DECL CLKC QP QN VALIDB RSTB SAMP EOC VDD VSS
*.ipin CLKS
*.ipin DECL
*.ipin OUTN
*.ipin OUTP
*.opin SAMP
*.opin RSTB
*.opin QP
*.opin CLKC
*.opin VALIDB
*.opin QN
*.opin EOC
*.iopin VDD
*.iopin VSS
xs1 CLKS VSS VSS VDD VDD SB1 sky130_fd_sc_hd__inv_1
xs2 SB1 VSS VSS VDD VDD SAMP sky130_fd_sc_hd__inv_4
xr3 CLKS VSS VSS VDD VDD RSTB sky130_fd_sc_hd__inv_4
xsd RSTB VSS VSS VDD VDD SAMPD sky130_fd_sc_hd__inv_1
xrun SAMPD DECL VSS VSS VDD VDD RUN sky130_fd_sc_hd__nor2_1
xqp OUTN VSS VSS VDD VDD QP sky130_fd_sc_hd__inv_4
xv OUTN OUTP VSS VSS VDD VDD VALID sky130_fd_sc_hd__nand2_1
xqn OUTP VSS VSS VDD VDD QN sky130_fd_sc_hd__inv_4
xvb VALID VSS VSS VDD VDD VALIDB sky130_fd_sc_hd__inv_4
xd1 VALIDB VSS VSS VDD VDD DL1 sky130_fd_sc_hd__inv_1
xd2 DL1 VSS VSS VDD VDD VD sky130_fd_sc_hd__inv_1
xg RUN VD VALIDB VSS VSS VDD VDD CLKCB sky130_fd_sc_hd__nand3_1
xgb CLKCB VSS VSS VDD VDD CLKC sky130_fd_sc_hd__inv_4
xe DECL VSS VSS VDD VDD EOC sky130_fd_sc_hd__buf_4
.ends


* expanding   symbol:  sar10_slice.sym # of pins=15
** sym_path: xschem/sar10_slice.sym
** sch_path: xschem/sar10_slice.sch
.subckt sar10_slice TPREV QP QN VALIDB RSTB EOC T DEC DP DPB DN DNB B VDD VSS
*.ipin QP
*.ipin TPREV
*.ipin RSTB
*.ipin QN
*.ipin VALIDB
*.ipin EOC
*.opin B
*.opin DP
*.opin DPB
*.opin DEC
*.opin T
*.opin DN
*.opin DNB
*.iopin VDD
*.iopin VSS
xlpb QP TPREV TB LP VSS VSS VDD VDD LPB sky130_fd_sc_hd__a31oi_1
xlp LPB RSTB VSS VSS VDD VDD LP sky130_fd_sc_hd__nor2b_1
xlnb QN TPREV TB LN VSS VSS VDD VDD LNB sky130_fd_sc_hd__a31oi_1
xln LNB RSTB VSS VSS VDD VDD LN sky130_fd_sc_hd__nor2b_1
xdec LPB LNB VSS VSS VDD VDD DEC sky130_fd_sc_hd__nand2_1
xst DEC VALIDB TB VSS VSS VDD VDD STB sky130_fd_sc_hd__nand3_1
xt STB TB VSS VSS VDD VDD T sky130_fd_sc_hd__nand2_1
xtb T DEC VSS VSS VDD VDD TB sky130_fd_sc_hd__nand2_1
xb EOC LP VSS VSS VDD VDD B sky130_fd_sc_hd__dfxtp_1
xgdp LPB VSS VSS VDD VDD DP sky130_fd_sc_hd__inv_4
xadpb LPB VSS VSS VDD VDD ADPB sky130_fd_sc_hd__inv_1
xgdpb ADPB VSS VSS VDD VDD DPB sky130_fd_sc_hd__inv_4
xgdn LNB VSS VSS VDD VDD DN sky130_fd_sc_hd__inv_4
xadnb LNB VSS VSS VDD VDD ADNB sky130_fd_sc_hd__inv_1
xgdnb ADNB VSS VSS VDD VDD DNB sky130_fd_sc_hd__inv_4
.ends

.end
